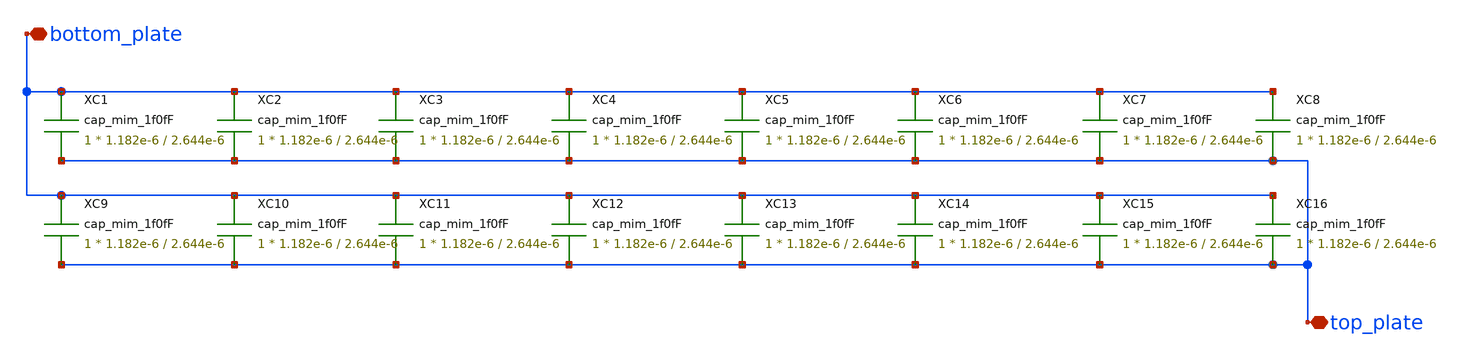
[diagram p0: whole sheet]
** sch_path: CDAC/16C.sch
**.subckt 16C bottom_plate top_plate
*.iopin bottom_plate
*.iopin top_plate
XC1 bottom_plate top_plate cap_mim_1f0fF c_width=1.182e-6 c_length=2.644e-6 m=1
XC2 bottom_plate top_plate cap_mim_1f0fF c_width=1.182e-6 c_length=2.644e-6 m=1
XC3 bottom_plate top_plate cap_mim_1f0fF c_width=1.182e-6 c_length=2.644e-6 m=1
XC4 bottom_plate top_plate cap_mim_1f0fF c_width=1.182e-6 c_length=2.644e-6 m=1
XC5 bottom_plate top_plate cap_mim_1f0fF c_width=1.182e-6 c_length=2.644e-6 m=1
XC6 bottom_plate top_plate cap_mim_1f0fF c_width=1.182e-6 c_length=2.644e-6 m=1
XC7 bottom_plate top_plate cap_mim_1f0fF c_width=1.182e-6 c_length=2.644e-6 m=1
XC8 bottom_plate top_plate cap_mim_1f0fF c_width=1.182e-6 c_length=2.644e-6 m=1
XC9 bottom_plate top_plate cap_mim_1f0fF c_width=1.182e-6 c_length=2.644e-6 m=1
XC10 bottom_plate top_plate cap_mim_1f0fF c_width=1.182e-6 c_length=2.644e-6 m=1
XC11 bottom_plate top_plate cap_mim_1f0fF c_width=1.182e-6 c_length=2.644e-6 m=1
XC12 bottom_plate top_plate cap_mim_1f0fF c_width=1.182e-6 c_length=2.644e-6 m=1
XC13 bottom_plate top_plate cap_mim_1f0fF c_width=1.182e-6 c_length=2.644e-6 m=1
XC14 bottom_plate top_plate cap_mim_1f0fF c_width=1.182e-6 c_length=2.644e-6 m=1
XC15 bottom_plate top_plate cap_mim_1f0fF c_width=1.182e-6 c_length=2.644e-6 m=1
XC16 bottom_plate top_plate cap_mim_1f0fF c_width=1.182e-6 c_length=2.644e-6 m=1
**.ends
.end
